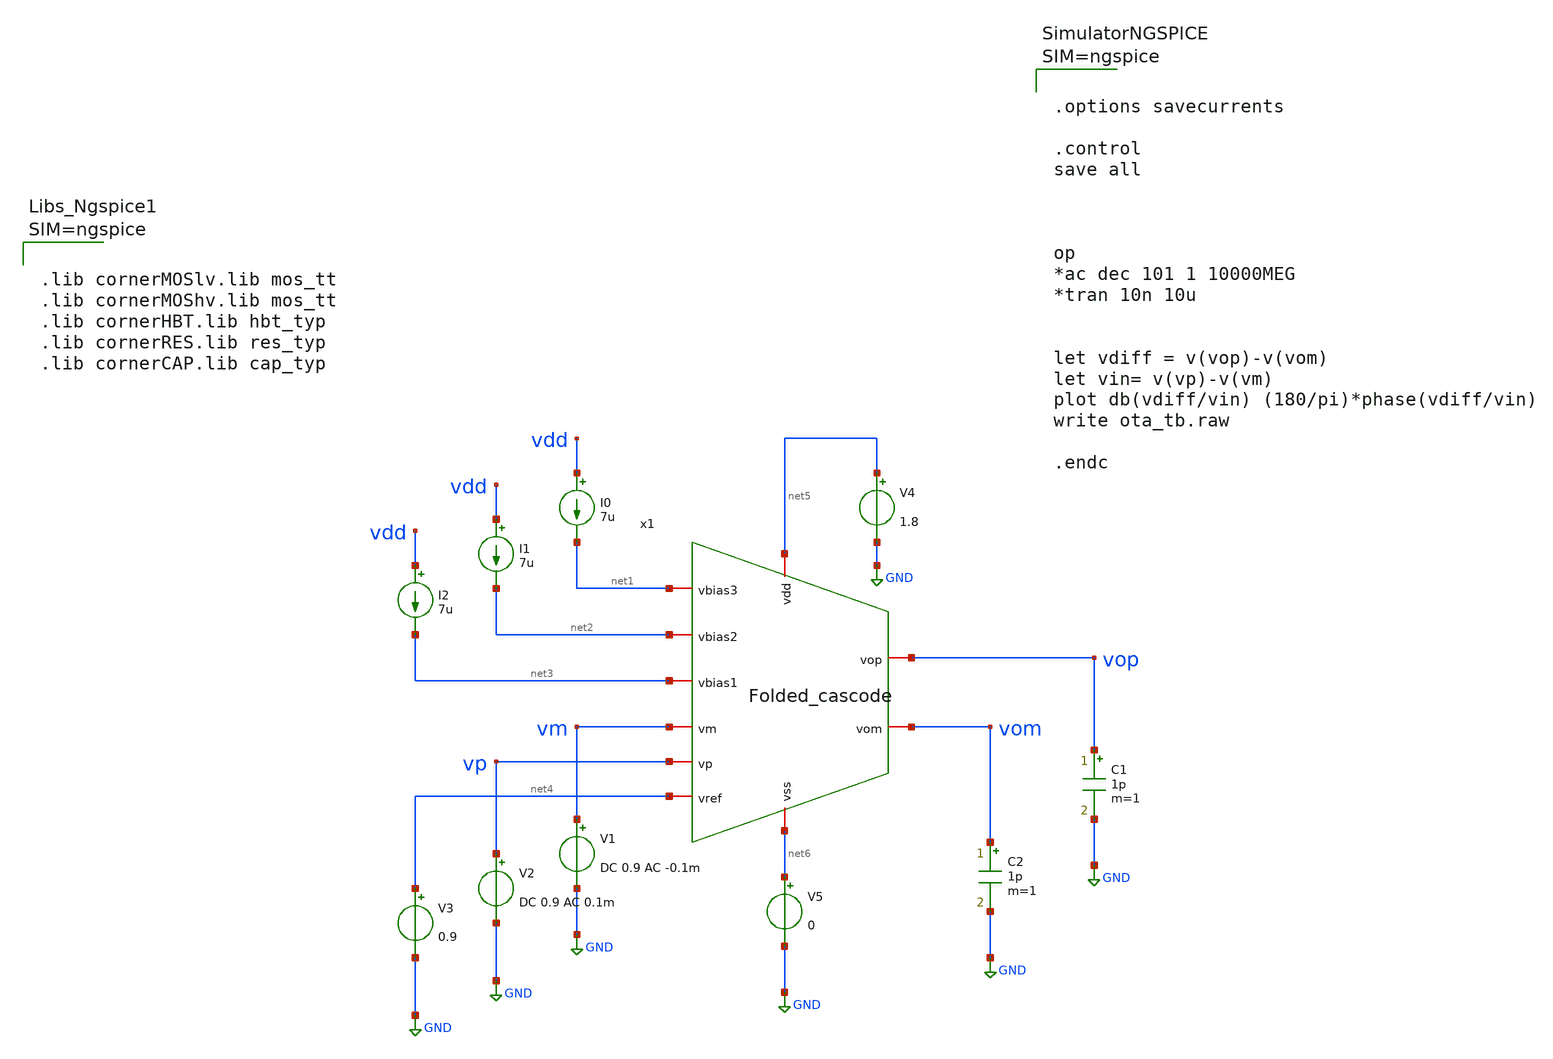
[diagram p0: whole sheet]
** sch_path: LVS/Unic_cass_final_design_lvs/Simulations/Opamp_design/testbench/ota_tb.sch
**.subckt ota_tb
x1 net1 net2 net3 vm vp net6 net5 net4 vop vom Folded_cascode
I0 vdd net1 7u
I1 vdd net2 7u
I2 vdd net3 7u
V1 vm GND DC 0.9 AC -0.1m
V2 vp GND DC 0.9 AC 0.1m
V3 net4 GND 0.9
V4 net5 GND 1.8
V5 net6 GND 0
C1 vop GND 1p m=1
C2 vom GND 1p m=1
**** begin user architecture code



.lib cornerMOSlv.lib mos_tt
.lib cornerMOShv.lib mos_tt
.lib cornerHBT.lib hbt_typ
.lib cornerRES.lib res_typ
.lib cornerCAP.lib cap_typ



**** end user architecture code
**.ends

* expanding   symbol:
*+  /home/designer/shared/unic_cass_2026/Unic_cass_final_design/Simulations/Opamp_design/Src/Folded_cascode.sym # of pins=10
** sym_path: LVS/Unic_cass_final_design_lvs/Simulations/Opamp_design/Src/Folded_cascode.sym
** sch_path: LVS/Unic_cass_final_design_lvs/Simulations/Opamp_design/Src/Folded_cascode.sch
.subckt Folded_cascode vbias3 vbias2 vbias1 vm vp vss vdd vref vop vom
*.iopin vbias3
*.iopin vbias2
*.iopin vbias1
*.iopin vm
*.iopin vp
*.iopin vss
*.iopin vdd
*.iopin vref
*.iopin vop
*.iopin vom
XM1 net3 vout vdd vdd sg13_lv_pmos w=1u l=5u ng=1 m=8 mm_ok=1
XM2 net1 vbias1 vss vss sg13_lv_nmos w=0.5u l=10u ng=1 m=4 mm_ok=1
XM4 net2 vm net1 vss sg13_lv_nmos w=2u l=10u ng=1 m=10 mm_ok=1
XM5 net3 vp net1 vss sg13_lv_nmos w=2u l=10u ng=1 m=10 mm_ok=1
XM3 net2 vout vdd vdd sg13_lv_pmos w=1u l=5u ng=1 m=8 mm_ok=1
XM6 vop vbiasp net2 vdd sg13_lv_pmos w=0.5u l=10u ng=1 m=16 mm_ok=1
XM7 vom vbiasp net3 vdd sg13_lv_pmos w=0.5u l=10u ng=1 m=16 mm_ok=1
XM8 vop vbias2 net7 vss sg13_lv_nmos w=1u l=10u ng=1 m=20 mm_ok=1
XM9 vom vbias2 net8 vss sg13_lv_nmos w=1u l=10u ng=1 m=20 mm_ok=1
XM10 net7 vbias1 vss vss sg13_lv_nmos w=0.5u l=10u ng=1 m=4 mm_ok=1
XM11 net8 vbias1 vss vss sg13_lv_nmos w=0.5u l=10u ng=1 m=4 mm_ok=1
XM12 net6 vom net4 vss sg13_lv_nmos w=0.5u l=10u ng=1 m=10 mm_ok=1
XM13 vout vref net4 vss sg13_lv_nmos w=0.5u l=10u ng=1 m=10 mm_ok=1
XM14 net6 vop net5 vss sg13_lv_nmos w=0.5u l=10u ng=1 m=10 mm_ok=1
XM15 vout vref net5 vss sg13_lv_nmos w=0.5u l=10u ng=1 m=10 mm_ok=1
XM16 net4 vbias1 vss vss sg13_lv_nmos w=0.5u l=10u ng=1 m=2 mm_ok=1
XM17 net5 vbias1 vss vss sg13_lv_nmos w=0.5u l=10u ng=1 m=2 mm_ok=1
XM18 net6 net6 vdd vdd sg13_lv_pmos w=1u l=10u ng=1 m=2 mm_ok=1
XM19 vout net6 vdd vdd sg13_lv_pmos w=1u l=10u ng=1 m=2 mm_ok=1
XM20 vbiasp vbiasp vdd vdd sg13_lv_pmos w=0.5u l=10u ng=1 m=6 mm_ok=1
XM21 vbias3 vbias3 vss vss sg13_lv_nmos w=0.6u l=1u ng=1 m=2 mm_ok=1
XM22 vbiasp vbias3 vss vss sg13_lv_nmos w=0.6u l=1u ng=1 m=2 mm_ok=1
XM23 vbias2 vbias2 vss vss sg13_lv_nmos w=1u l=10u ng=1 m=2 mm_ok=1
XM24 vbias1 vbias1 vss vss sg13_lv_nmos w=0.5u l=10u ng=1 m=20 mm_ok=1
XC1 vout vop cap_cmim w=10.0e-6 l=10.0e-6 m=8 mm_ok=1
XC2 vout vom cap_cmim w=10.0e-6 l=10.0e-6 m=8 mm_ok=1
XM25 vss vss vss vss sg13_lv_nmos w=0.5u l=10u ng=1 m=8 mm_ok=1
XM26 vss vss vss vss sg13_lv_nmos w=0.5u l=0.5u ng=1 m=22 mm_ok=1
XM27 vss vss vss vss sg13_lv_nmos w=0.5u l=10u ng=1 m=4 mm_ok=1
XM28 vss vss vss vss sg13_lv_nmos w=1u l=0.5u ng=1 m=42 mm_ok=1
XM29 vss vss vss vss sg13_lv_nmos w=0.5u l=0.5u ng=1 m=4 mm_ok=1
XM30 vss vss vss vss sg13_lv_nmos w=0.5u l=10u ng=1 m=4 mm_ok=1
XM31 vss vss vss vss sg13_lv_nmos w=2u l=0.5u ng=1 m=20 mm_ok=1
XM33 vss vss vss vss sg13_lv_nmos w=0.5u l=10u ng=1 m=8 mm_ok=1
XM34 vss vss vss vss sg13_lv_nmos w=0.5u l=0.5u ng=1 m=24 mm_ok=1
XM35 vdd vdd vdd vdd sg13_lv_pmos w=0.5u l=0.5u ng=1 m=44 mm_ok=1
XM36 vdd vdd vdd vdd sg13_lv_pmos w=0.5u l=10u ng=1 m=6 mm_ok=1
XM37 vdd vdd vdd vdd sg13_lv_pmos w=0.5u l=0.5u ng=1 m=4 mm_ok=1
XM38 vdd vdd vdd vdd sg13_lv_pmos w=0.5u l=5u ng=1 m=4 mm_ok=1
XM39 vdd vdd vdd vdd sg13_lv_pmos w=1u l=0.5u ng=1 m=16 mm_ok=1
XM40 vss vss vss vss sg13_lv_nmos w=0.6u l=1u ng=1 m=2 mm_ok=1
XM41 vss vss vss vss sg13_lv_nmos w=0.6u l=0.5u ng=1 m=12 mm_ok=1
XM42 vdd vdd vdd vdd sg13_lv_pmos w=0.5u l=0.5u ng=1 m=4 mm_ok=1
XM43 vdd vdd vdd vdd sg13_lv_pmos w=0.5u l=10u ng=1 m=2 mm_ok=1
XM44 vdd vdd vdd vdd sg13_lv_pmos w=1u l=0.5u ng=1 m=8 mm_ok=1
XM45 vss vss vss vss sg13_lv_nmos w=0.5u l=0.5u ng=1 m=4 mm_ok=1
.ends

.GLOBAL GND
**** begin user architecture code



.options savecurrents

.control
save all



op
*ac dec 101 1 10000MEG
*tran 10n 10u


let vdiff = v(vop)-v(vom)
let vin= v(vp)-v(vm)
plot db(vdiff/vin) (180/pi)*phase(vdiff/vin)
write ota_tb.raw

.endc



**** end user architecture code
.end
